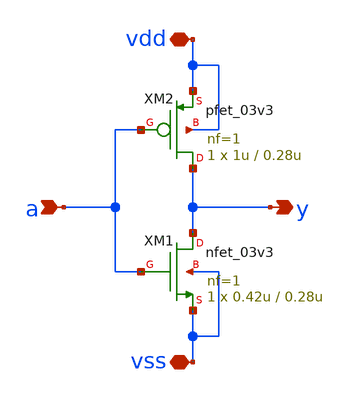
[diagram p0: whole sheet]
** sch_path: member_project/ice458/dynamic_comparator/xschem/inv.sch
**.subckt inv vdd vss a y
*.iopin vdd
*.iopin vss
*.ipin a
*.opin y
XM1 y a vss vss nfet_03v3 L=0.28u W=0.42u nf=1 ad='int((nf+1)/2) * W/nf * 0.18u' as='int((nf+2)/2) * W/nf * 0.18u'
+ pd='2*int((nf+1)/2) * (W/nf + 0.18u)' ps='2*int((nf+2)/2) * (W/nf + 0.18u)' nrd='0.18u / W' nrs='0.18u / W'
+ sa=0 sb=0 sd=0 m=1
XM2 y a vdd vdd pfet_03v3 L=0.28u W=1u nf=1 ad='int((nf+1)/2) * W/nf * 0.18u' as='int((nf+2)/2) * W/nf * 0.18u'
+ pd='2*int((nf+1)/2) * (W/nf + 0.18u)' ps='2*int((nf+2)/2) * (W/nf + 0.18u)' nrd='0.18u / W' nrs='0.18u / W'
+ sa=0 sb=0 sd=0 m=1
**.ends
.end
